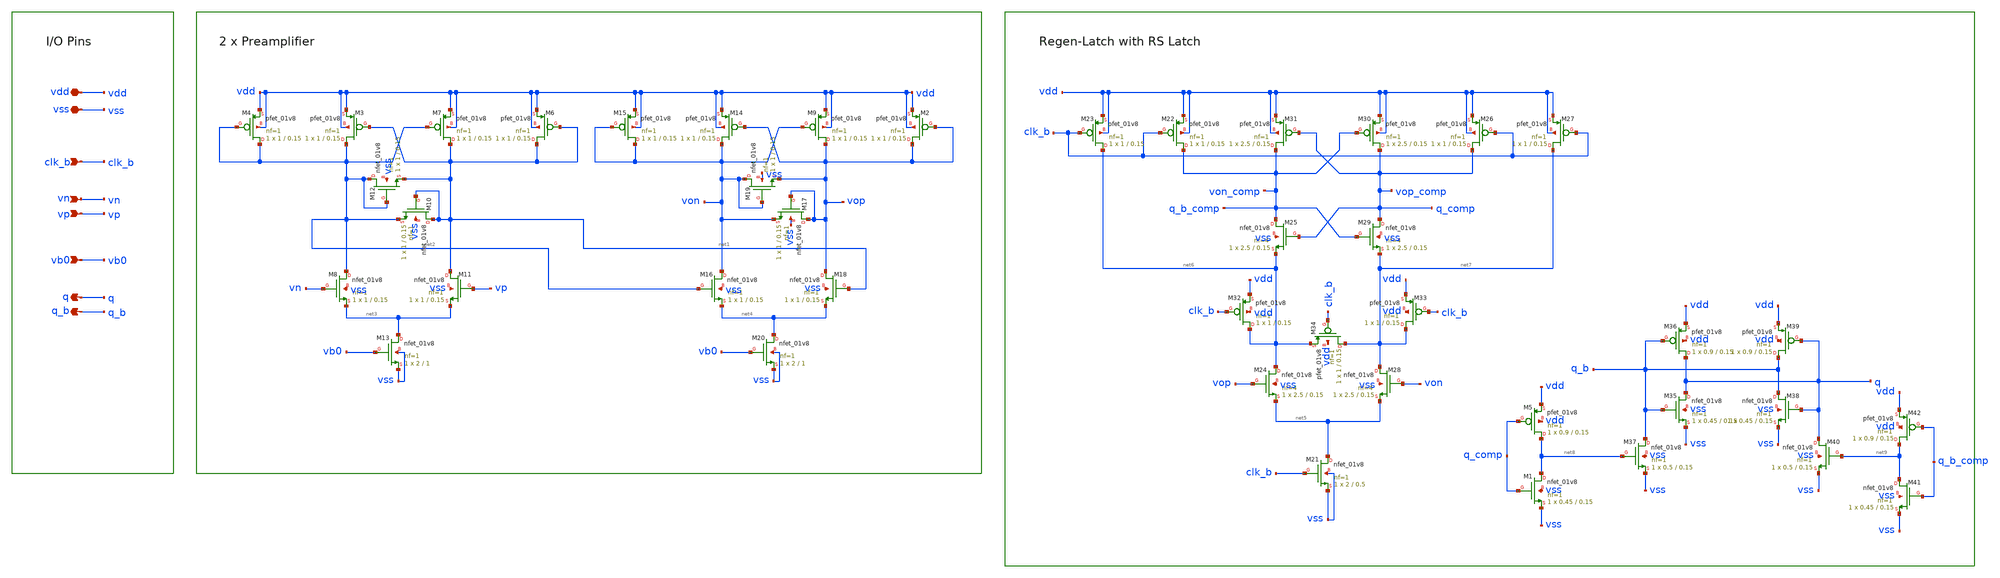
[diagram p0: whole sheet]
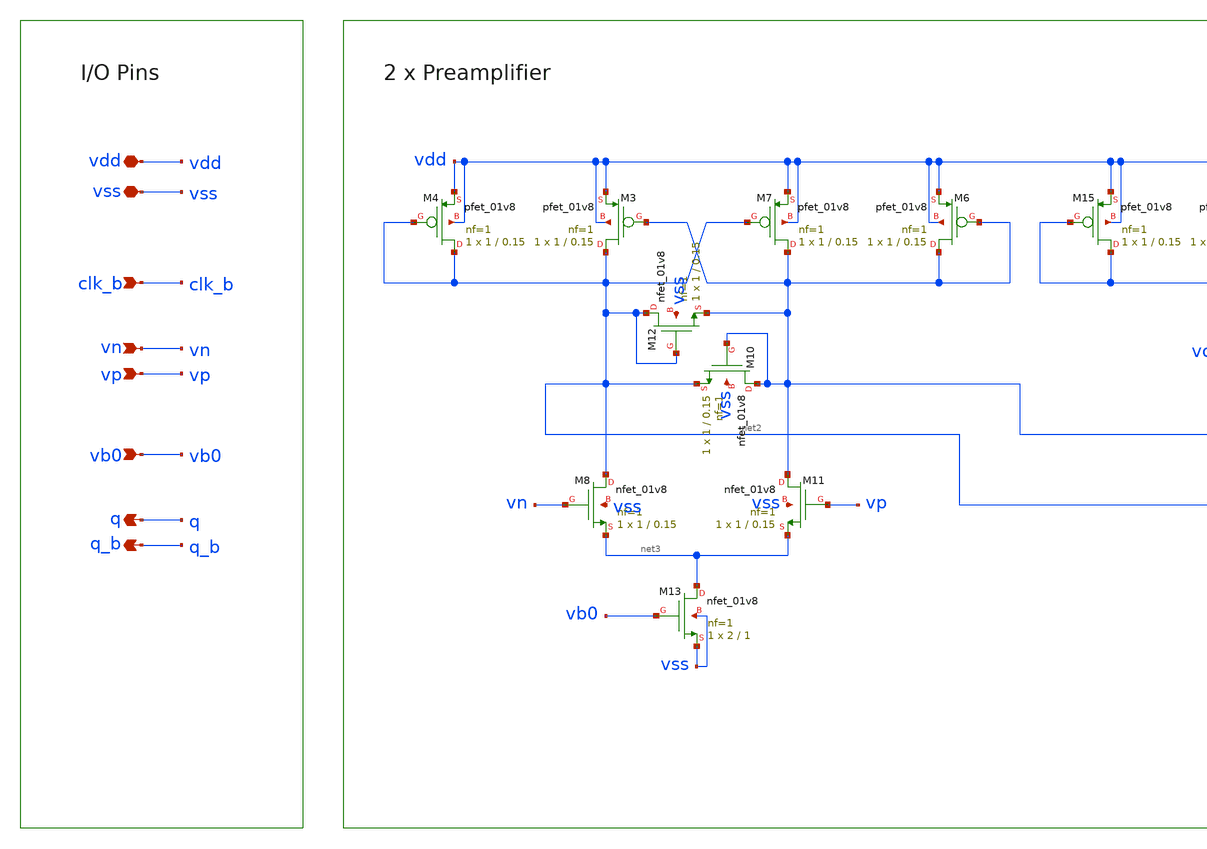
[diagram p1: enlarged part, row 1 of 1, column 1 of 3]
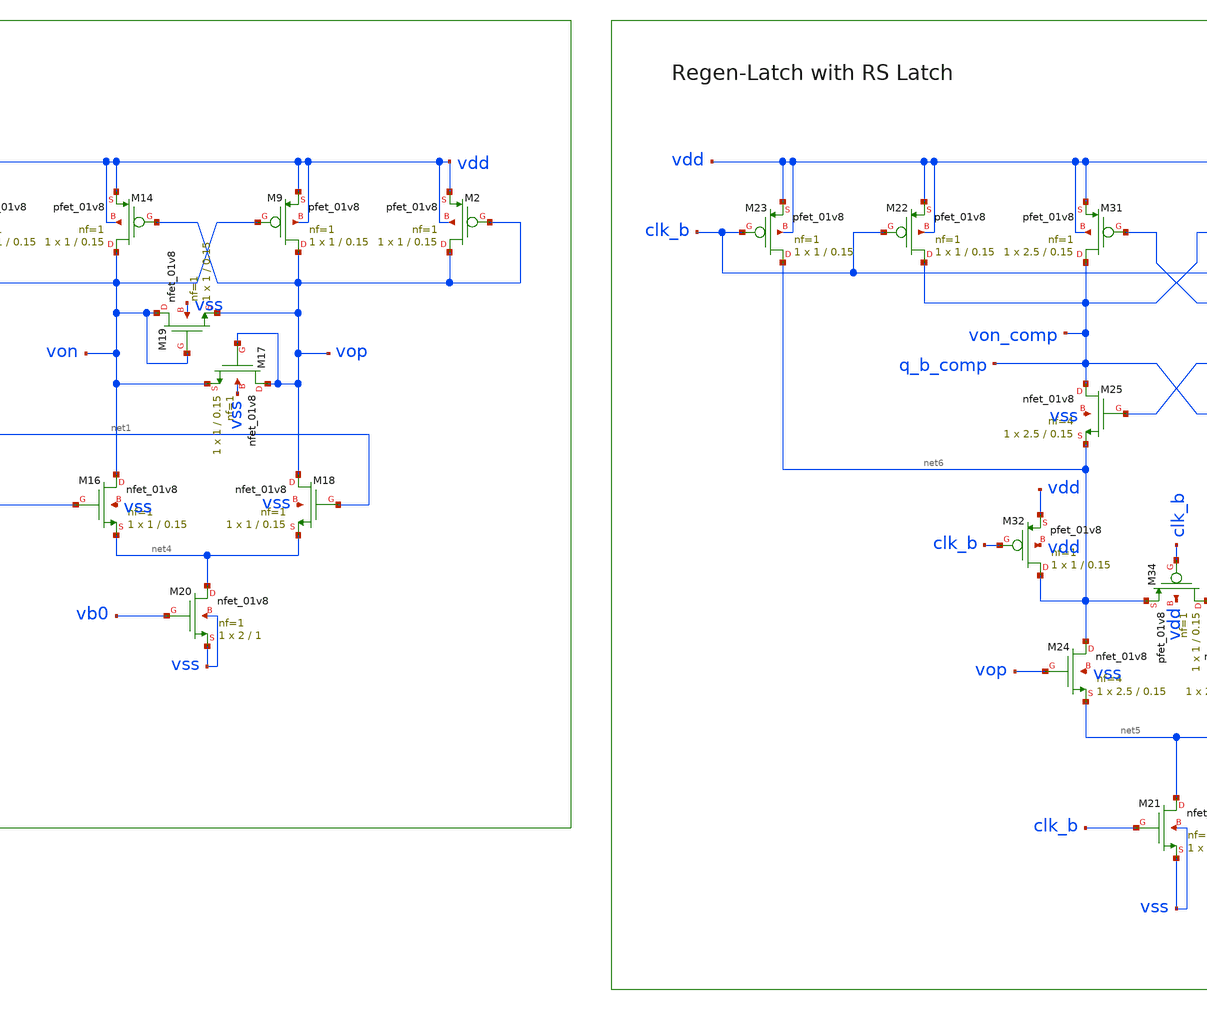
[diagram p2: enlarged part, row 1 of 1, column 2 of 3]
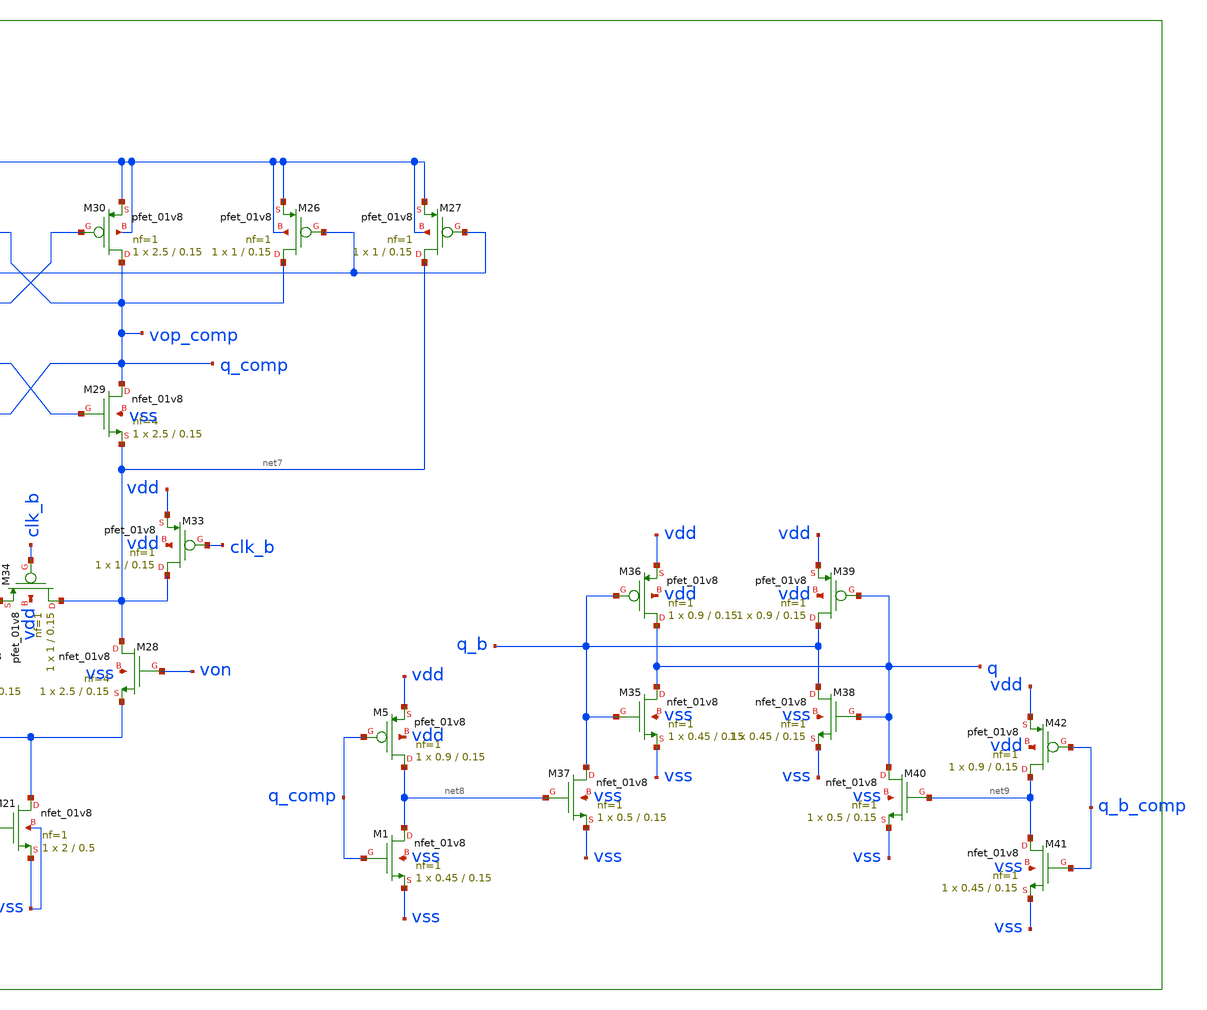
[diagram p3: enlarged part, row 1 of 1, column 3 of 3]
** sch_path: xschem/comparator.sch
**.subckt comparator vp vn vdd vss q q_b clk_b vb0
*.ipin vp
*.ipin vn
*.iopin vdd
*.iopin vss
*.opin q
*.opin q_b
*.ipin clk_b
*.ipin vb0
XM6 net1 net1 vdd vdd sky130_fd_pr__pfet_01v8 L=0.15 W=1 nf=1 ad='int((nf+1)/2) * W/nf * 0.29' as='int((nf+2)/2) * W/nf * 0.29'
+ pd='2*int((nf+1)/2) * (W/nf + 0.29)' ps='2*int((nf+2)/2) * (W/nf + 0.29)' nrd='0.29 / W' nrs='0.29 / W'
+ sa=0 sb=0 sd=0 mult=1 m=1
XM7 net1 net2 vdd vdd sky130_fd_pr__pfet_01v8 L=0.15 W=1 nf=1 ad='int((nf+1)/2) * W/nf * 0.29' as='int((nf+2)/2) * W/nf * 0.29'
+ pd='2*int((nf+1)/2) * (W/nf + 0.29)' ps='2*int((nf+2)/2) * (W/nf + 0.29)' nrd='0.29 / W' nrs='0.29 / W'
+ sa=0 sb=0 sd=0 mult=1 m=1
XM3 net2 net1 vdd vdd sky130_fd_pr__pfet_01v8 L=0.15 W=1 nf=1 ad='int((nf+1)/2) * W/nf * 0.29' as='int((nf+2)/2) * W/nf * 0.29'
+ pd='2*int((nf+1)/2) * (W/nf + 0.29)' ps='2*int((nf+2)/2) * (W/nf + 0.29)' nrd='0.29 / W' nrs='0.29 / W'
+ sa=0 sb=0 sd=0 mult=1 m=1
XM4 net2 net2 vdd vdd sky130_fd_pr__pfet_01v8 L=0.15 W=1 nf=1 ad='int((nf+1)/2) * W/nf * 0.29' as='int((nf+2)/2) * W/nf * 0.29'
+ pd='2*int((nf+1)/2) * (W/nf + 0.29)' ps='2*int((nf+2)/2) * (W/nf + 0.29)' nrd='0.29 / W' nrs='0.29 / W'
+ sa=0 sb=0 sd=0 mult=1 m=1
XM8 net2 vn net3 vss sky130_fd_pr__nfet_01v8 L=0.15 W=1 nf=1 ad='int((1 + 1)/2) * 1 / 1 * 0.29' as='int((1 + 2)/2) * 1 / 1 * 0.29'
+ pd='2*int((1 + 1)/2) * (1 / 1 + 0.29)' ps='2*int((1 + 2)/2) * (1 / 1 + 0.29)' nrd='0.29 / 1 ' nrs='0.29 / 1 '
+ sa=0 sb=0 sd=0 mult=1 m=1
XM10 net1 net1 net2 vss sky130_fd_pr__nfet_01v8 L=0.15 W=1 nf=1 ad='int((1 + 1)/2) * 1 / 1 * 0.29' as='int((1 + 2)/2) * 1 / 1 * 0.29'
+ pd='2*int((1 + 1)/2) * (1 / 1 + 0.29)' ps='2*int((1 + 2)/2) * (1 / 1 + 0.29)' nrd='0.29 / 1 ' nrs='0.29 / 1 '
+ sa=0 sb=0 sd=0 mult=1 m=1
XM11 net1 vp net3 vss sky130_fd_pr__nfet_01v8 L=0.15 W=1 nf=1 ad='int((1 + 1)/2) * 1 / 1 * 0.29' as='int((1 + 2)/2) * 1 / 1 * 0.29'
+ pd='2*int((1 + 1)/2) * (1 / 1 + 0.29)' ps='2*int((1 + 2)/2) * (1 / 1 + 0.29)' nrd='0.29 / 1 ' nrs='0.29 / 1 '
+ sa=0 sb=0 sd=0 mult=1 m=1
XM12 net2 net2 net1 vss sky130_fd_pr__nfet_01v8 L=0.15 W=1 nf=1 ad='int((1 + 1)/2) * 1 / 1 * 0.29' as='int((1 + 2)/2) * 1 / 1 * 0.29'
+ pd='2*int((1 + 1)/2) * (1 / 1 + 0.29)' ps='2*int((1 + 2)/2) * (1 / 1 + 0.29)' nrd='0.29 / 1 ' nrs='0.29 / 1 '
+ sa=0 sb=0 sd=0 mult=1 m=1
XM13 net3 vb0 vss vss sky130_fd_pr__nfet_01v8 L=1 W=2 nf=1 ad='int((1 + 1)/2) * 2 / 1 * 0.29' as='int((1 + 2)/2) * 2 / 1 * 0.29'
+ pd='2*int((1 + 1)/2) * (2 / 1 + 0.29)' ps='2*int((1 + 2)/2) * (2 / 1 + 0.29)' nrd='0.29 / 2 ' nrs='0.29 / 2 '
+ sa=0 sb=0 sd=0 mult=1 m=1
XM2 vop vop vdd vdd sky130_fd_pr__pfet_01v8 L=0.15 W=1 nf=1 ad='int((nf+1)/2) * W/nf * 0.29' as='int((nf+2)/2) * W/nf * 0.29'
+ pd='2*int((nf+1)/2) * (W/nf + 0.29)' ps='2*int((nf+2)/2) * (W/nf + 0.29)' nrd='0.29 / W' nrs='0.29 / W'
+ sa=0 sb=0 sd=0 mult=1 m=1
XM9 vop von vdd vdd sky130_fd_pr__pfet_01v8 L=0.15 W=1 nf=1 ad='int((nf+1)/2) * W/nf * 0.29' as='int((nf+2)/2) * W/nf * 0.29'
+ pd='2*int((nf+1)/2) * (W/nf + 0.29)' ps='2*int((nf+2)/2) * (W/nf + 0.29)' nrd='0.29 / W' nrs='0.29 / W'
+ sa=0 sb=0 sd=0 mult=1 m=1
XM14 von vop vdd vdd sky130_fd_pr__pfet_01v8 L=0.15 W=1 nf=1 ad='int((nf+1)/2) * W/nf * 0.29' as='int((nf+2)/2) * W/nf * 0.29'
+ pd='2*int((nf+1)/2) * (W/nf + 0.29)' ps='2*int((nf+2)/2) * (W/nf + 0.29)' nrd='0.29 / W' nrs='0.29 / W'
+ sa=0 sb=0 sd=0 mult=1 m=1
XM15 von von vdd vdd sky130_fd_pr__pfet_01v8 L=0.15 W=1 nf=1 ad='int((nf+1)/2) * W/nf * 0.29' as='int((nf+2)/2) * W/nf * 0.29'
+ pd='2*int((nf+1)/2) * (W/nf + 0.29)' ps='2*int((nf+2)/2) * (W/nf + 0.29)' nrd='0.29 / W' nrs='0.29 / W'
+ sa=0 sb=0 sd=0 mult=1 m=1
XM16 von net2 net4 vss sky130_fd_pr__nfet_01v8 L=0.15 W=1 nf=1 ad='int((1 + 1)/2) * 1 / 1 * 0.29' as='int((1 + 2)/2) * 1 / 1 * 0.29'
+ pd='2*int((1 + 1)/2) * (1 / 1 + 0.29)' ps='2*int((1 + 2)/2) * (1 / 1 + 0.29)' nrd='0.29 / 1 ' nrs='0.29 / 1 '
+ sa=0 sb=0 sd=0 mult=1 m=1
XM17 vop vop von vss sky130_fd_pr__nfet_01v8 L=0.15 W=1 nf=1 ad='int((1 + 1)/2) * 1 / 1 * 0.29' as='int((1 + 2)/2) * 1 / 1 * 0.29'
+ pd='2*int((1 + 1)/2) * (1 / 1 + 0.29)' ps='2*int((1 + 2)/2) * (1 / 1 + 0.29)' nrd='0.29 / 1 ' nrs='0.29 / 1 '
+ sa=0 sb=0 sd=0 mult=1 m=1
XM18 vop net1 net4 vss sky130_fd_pr__nfet_01v8 L=0.15 W=1 nf=1 ad='int((1 + 1)/2) * 1 / 1 * 0.29' as='int((1 + 2)/2) * 1 / 1 * 0.29'
+ pd='2*int((1 + 1)/2) * (1 / 1 + 0.29)' ps='2*int((1 + 2)/2) * (1 / 1 + 0.29)' nrd='0.29 / 1 ' nrs='0.29 / 1 '
+ sa=0 sb=0 sd=0 mult=1 m=1
XM19 von von vop vss sky130_fd_pr__nfet_01v8 L=0.15 W=1 nf=1 ad='int((1 + 1)/2) * 1 / 1 * 0.29' as='int((1 + 2)/2) * 1 / 1 * 0.29'
+ pd='2*int((1 + 1)/2) * (1 / 1 + 0.29)' ps='2*int((1 + 2)/2) * (1 / 1 + 0.29)' nrd='0.29 / 1 ' nrs='0.29 / 1 '
+ sa=0 sb=0 sd=0 mult=1 m=1
XM20 net4 vb0 vss vss sky130_fd_pr__nfet_01v8 L=1 W=2 nf=1 ad='int((1 + 1)/2) * 2 / 1 * 0.29' as='int((1 + 2)/2) * 2 / 1 * 0.29'
+ pd='2*int((1 + 1)/2) * (2 / 1 + 0.29)' ps='2*int((1 + 2)/2) * (2 / 1 + 0.29)' nrd='0.29 / 2 ' nrs='0.29 / 2 '
+ sa=0 sb=0 sd=0 mult=1 m=1
XM21 net5 clk_b vss vss sky130_fd_pr__nfet_01v8 L=0.5 W=2 nf=1 ad='int((nf+1)/2) * W/nf * 0.29' as='int((nf+2)/2) * W/nf * 0.29'
+ pd='2*int((nf+1)/2) * (W/nf + 0.29)' ps='2*int((nf+2)/2) * (W/nf + 0.29)' nrd='0.29 / W' nrs='0.29 / W'
+ sa=0 sb=0 sd=0 mult=1 m=1
XM22 q_b_comp clk_b vdd vdd sky130_fd_pr__pfet_01v8 L=0.15 W=1 nf=1 ad='int((nf+1)/2) * W/nf * 0.29'
+ as='int((nf+2)/2) * W/nf * 0.29' pd='2*int((nf+1)/2) * (W/nf + 0.29)' ps='2*int((nf+2)/2) * (W/nf + 0.29)'
+ nrd='0.29 / W' nrs='0.29 / W' sa=0 sb=0 sd=0 mult=1 m=1
XM23 net6 clk_b vdd vdd sky130_fd_pr__pfet_01v8 L=0.15 W=1 nf=1 ad='int((nf+1)/2) * W/nf * 0.29' as='int((nf+2)/2) * W/nf * 0.29'
+ pd='2*int((nf+1)/2) * (W/nf + 0.29)' ps='2*int((nf+2)/2) * (W/nf + 0.29)' nrd='0.29 / W' nrs='0.29 / W'
+ sa=0 sb=0 sd=0 mult=1 m=1
XM24 net6 vop net5 vss sky130_fd_pr__nfet_01v8 L=0.15 W=2.5 nf=4 ad='int((nf+1)/2) * W/nf * 0.29' as='int((nf+2)/2) * W/nf * 0.29'
+ pd='2*int((nf+1)/2) * (W/nf + 0.29)' ps='2*int((nf+2)/2) * (W/nf + 0.29)' nrd='0.29 / W' nrs='0.29 / W'
+ sa=0 sb=0 sd=0 mult=1 m=1
XM25 q_b_comp q_comp net6 vss sky130_fd_pr__nfet_01v8 L=0.15 W=2.5 nf=4 ad='int((nf+1)/2) * W/nf * 0.29'
+ as='int((nf+2)/2) * W/nf * 0.29' pd='2*int((nf+1)/2) * (W/nf + 0.29)' ps='2*int((nf+2)/2) * (W/nf + 0.29)'
+ nrd='0.29 / W' nrs='0.29 / W' sa=0 sb=0 sd=0 mult=1 m=1
XM26 q_comp clk_b vdd vdd sky130_fd_pr__pfet_01v8 L=0.15 W=1 nf=1 ad='int((nf+1)/2) * W/nf * 0.29' as='int((nf+2)/2) * W/nf * 0.29'
+ pd='2*int((nf+1)/2) * (W/nf + 0.29)' ps='2*int((nf+2)/2) * (W/nf + 0.29)' nrd='0.29 / W' nrs='0.29 / W'
+ sa=0 sb=0 sd=0 mult=1 m=1
XM27 net7 clk_b vdd vdd sky130_fd_pr__pfet_01v8 L=0.15 W=1 nf=1 ad='int((nf+1)/2) * W/nf * 0.29' as='int((nf+2)/2) * W/nf * 0.29'
+ pd='2*int((nf+1)/2) * (W/nf + 0.29)' ps='2*int((nf+2)/2) * (W/nf + 0.29)' nrd='0.29 / W' nrs='0.29 / W'
+ sa=0 sb=0 sd=0 mult=1 m=1
XM28 net7 von net5 vss sky130_fd_pr__nfet_01v8 L=0.15 W=2.5 nf=4 ad='int((nf+1)/2) * W/nf * 0.29' as='int((nf+2)/2) * W/nf * 0.29'
+ pd='2*int((nf+1)/2) * (W/nf + 0.29)' ps='2*int((nf+2)/2) * (W/nf + 0.29)' nrd='0.29 / W' nrs='0.29 / W'
+ sa=0 sb=0 sd=0 mult=1 m=1
XM29 q_comp q_b_comp net7 vss sky130_fd_pr__nfet_01v8 L=0.15 W=2.5 nf=4 ad='int((nf+1)/2) * W/nf * 0.29'
+ as='int((nf+2)/2) * W/nf * 0.29' pd='2*int((nf+1)/2) * (W/nf + 0.29)' ps='2*int((nf+2)/2) * (W/nf + 0.29)'
+ nrd='0.29 / W' nrs='0.29 / W' sa=0 sb=0 sd=0 mult=1 m=1
XM30 q_comp q_b_comp vdd vdd sky130_fd_pr__pfet_01v8 L=0.15 W=2.5 nf=1 ad='int((nf+1)/2) * W/nf * 0.29'
+ as='int((nf+2)/2) * W/nf * 0.29' pd='2*int((nf+1)/2) * (W/nf + 0.29)' ps='2*int((nf+2)/2) * (W/nf + 0.29)'
+ nrd='0.29 / W' nrs='0.29 / W' sa=0 sb=0 sd=0 mult=1 m=1
XM31 q_b_comp q_comp vdd vdd sky130_fd_pr__pfet_01v8 L=0.15 W=2.5 nf=1 ad='int((nf+1)/2) * W/nf * 0.29'
+ as='int((nf+2)/2) * W/nf * 0.29' pd='2*int((nf+1)/2) * (W/nf + 0.29)' ps='2*int((nf+2)/2) * (W/nf + 0.29)'
+ nrd='0.29 / W' nrs='0.29 / W' sa=0 sb=0 sd=0 mult=1 m=1
XM32 net6 clk_b vdd vdd sky130_fd_pr__pfet_01v8 L=0.15 W=1 nf=1 ad='int((nf+1)/2) * W/nf * 0.29' as='int((nf+2)/2) * W/nf * 0.29'
+ pd='2*int((nf+1)/2) * (W/nf + 0.29)' ps='2*int((nf+2)/2) * (W/nf + 0.29)' nrd='0.29 / W' nrs='0.29 / W'
+ sa=0 sb=0 sd=0 mult=1 m=1
XM33 net7 clk_b vdd vdd sky130_fd_pr__pfet_01v8 L=0.15 W=1 nf=1 ad='int((nf+1)/2) * W/nf * 0.29' as='int((nf+2)/2) * W/nf * 0.29'
+ pd='2*int((nf+1)/2) * (W/nf + 0.29)' ps='2*int((nf+2)/2) * (W/nf + 0.29)' nrd='0.29 / W' nrs='0.29 / W'
+ sa=0 sb=0 sd=0 mult=1 m=1
XM34 net7 clk_b net6 vdd sky130_fd_pr__pfet_01v8 L=0.15 W=1 nf=1 ad='int((nf+1)/2) * W/nf * 0.29' as='int((nf+2)/2) * W/nf * 0.29'
+ pd='2*int((nf+1)/2) * (W/nf + 0.29)' ps='2*int((nf+2)/2) * (W/nf + 0.29)' nrd='0.29 / W' nrs='0.29 / W'
+ sa=0 sb=0 sd=0 mult=1 m=1
XM35 q q_b vss vss sky130_fd_pr__nfet_01v8 L=0.15 W=0.45 nf=1 ad='int((1 + 1)/2) * 0.45 / 1 * 0.29' as='int((1 + 2)/2) * 0.45 / 1 * 0.29'
+ pd='2*int((1 + 1)/2) * (0.45 / 1 + 0.29)' ps='2*int((1 + 2)/2) * (0.45 / 1 + 0.29)' nrd='0.29 / 0.45 '
+ nrs='0.29 / 0.45 ' sa=0 sb=0 sd=0 mult=1 m=1
XM36 q q_b vdd vdd sky130_fd_pr__pfet_01v8 L=0.15 W=0.9 nf=1 ad='int((nf+1)/2) * W/nf * 0.29' as='int((nf+2)/2) * W/nf * 0.29'
+ pd='2*int((nf+1)/2) * (W/nf + 0.29)' ps='2*int((nf+2)/2) * (W/nf + 0.29)' nrd='0.29 / W' nrs='0.29 / W'
+ sa=0 sb=0 sd=0 mult=1 m=1
XM37 q_b net8 vss vss sky130_fd_pr__nfet_01v8 L=0.15 W=0.5 nf=1 ad='int((1 + 1)/2) * 0.5 / 1 * 0.29'
+ as='int((1 + 2)/2) * 0.5 / 1 * 0.29' pd='2*int((1 + 1)/2) * (0.5 / 1 + 0.29)' ps='2*int((1 + 2)/2) * (0.5 / 1 + 0.29)'
+ nrd='0.29 / 0.5 ' nrs='0.29 / 0.5 ' sa=0 sb=0 sd=0 mult=1 m=1
XM38 q_b q vss vss sky130_fd_pr__nfet_01v8 L=0.15 W=0.45 nf=1 ad='int((1 + 1)/2) * 0.45 / 1 * 0.29' as='int((1 + 2)/2) * 0.45 / 1 * 0.29'
+ pd='2*int((1 + 1)/2) * (0.45 / 1 + 0.29)' ps='2*int((1 + 2)/2) * (0.45 / 1 + 0.29)' nrd='0.29 / 0.45 '
+ nrs='0.29 / 0.45 ' sa=0 sb=0 sd=0 mult=1 m=1
XM39 q_b q vdd vdd sky130_fd_pr__pfet_01v8 L=0.15 W=0.9 nf=1 ad='int((nf+1)/2) * W/nf * 0.29' as='int((nf+2)/2) * W/nf * 0.29'
+ pd='2*int((nf+1)/2) * (W/nf + 0.29)' ps='2*int((nf+2)/2) * (W/nf + 0.29)' nrd='0.29 / W' nrs='0.29 / W'
+ sa=0 sb=0 sd=0 mult=1 m=1
XM40 q net9 vss vss sky130_fd_pr__nfet_01v8 L=0.15 W=0.5 nf=1 ad='int((1 + 1)/2) * 0.5 / 1 * 0.29' as='int((1 + 2)/2) * 0.5 / 1 * 0.29'
+ pd='2*int((1 + 1)/2) * (0.5 / 1 + 0.29)' ps='2*int((1 + 2)/2) * (0.5 / 1 + 0.29)' nrd='0.29 / 0.5 ' nrs='0.29 / 0.5 '
+ sa=0 sb=0 sd=0 mult=1 m=1
XM1 net8 q_comp vss vss sky130_fd_pr__nfet_01v8 L=0.15 W=0.45 nf=1 ad='int((1 + 1)/2) * 0.45 / 1 * 0.29'
+ as='int((1 + 2)/2) * 0.45 / 1 * 0.29' pd='2*int((1 + 1)/2) * (0.45 / 1 + 0.29)' ps='2*int((1 + 2)/2) * (0.45 / 1 + 0.29)'
+ nrd='0.29 / 0.45 ' nrs='0.29 / 0.45 ' sa=0 sb=0 sd=0 mult=1 m=1
XM5 net8 q_comp vdd vdd sky130_fd_pr__pfet_01v8 L=0.15 W=0.9 nf=1 ad='int((nf+1)/2) * W/nf * 0.29' as='int((nf+2)/2) * W/nf * 0.29'
+ pd='2*int((nf+1)/2) * (W/nf + 0.29)' ps='2*int((nf+2)/2) * (W/nf + 0.29)' nrd='0.29 / W' nrs='0.29 / W'
+ sa=0 sb=0 sd=0 mult=1 m=1
XM41 net9 q_b_comp vss vss sky130_fd_pr__nfet_01v8 L=0.15 W=0.45 nf=1 ad='int((1 + 1)/2) * 0.45 / 1 * 0.29'
+ as='int((1 + 2)/2) * 0.45 / 1 * 0.29' pd='2*int((1 + 1)/2) * (0.45 / 1 + 0.29)' ps='2*int((1 + 2)/2) * (0.45 / 1 + 0.29)'
+ nrd='0.29 / 0.45 ' nrs='0.29 / 0.45 ' sa=0 sb=0 sd=0 mult=1 m=1
XM42 net9 q_b_comp vdd vdd sky130_fd_pr__pfet_01v8 L=0.15 W=0.9 nf=1 ad='int((nf+1)/2) * W/nf * 0.29'
+ as='int((nf+2)/2) * W/nf * 0.29' pd='2*int((nf+1)/2) * (W/nf + 0.29)' ps='2*int((nf+2)/2) * (W/nf + 0.29)'
+ nrd='0.29 / W' nrs='0.29 / W' sa=0 sb=0 sd=0 mult=1 m=1
**.ends
.end
